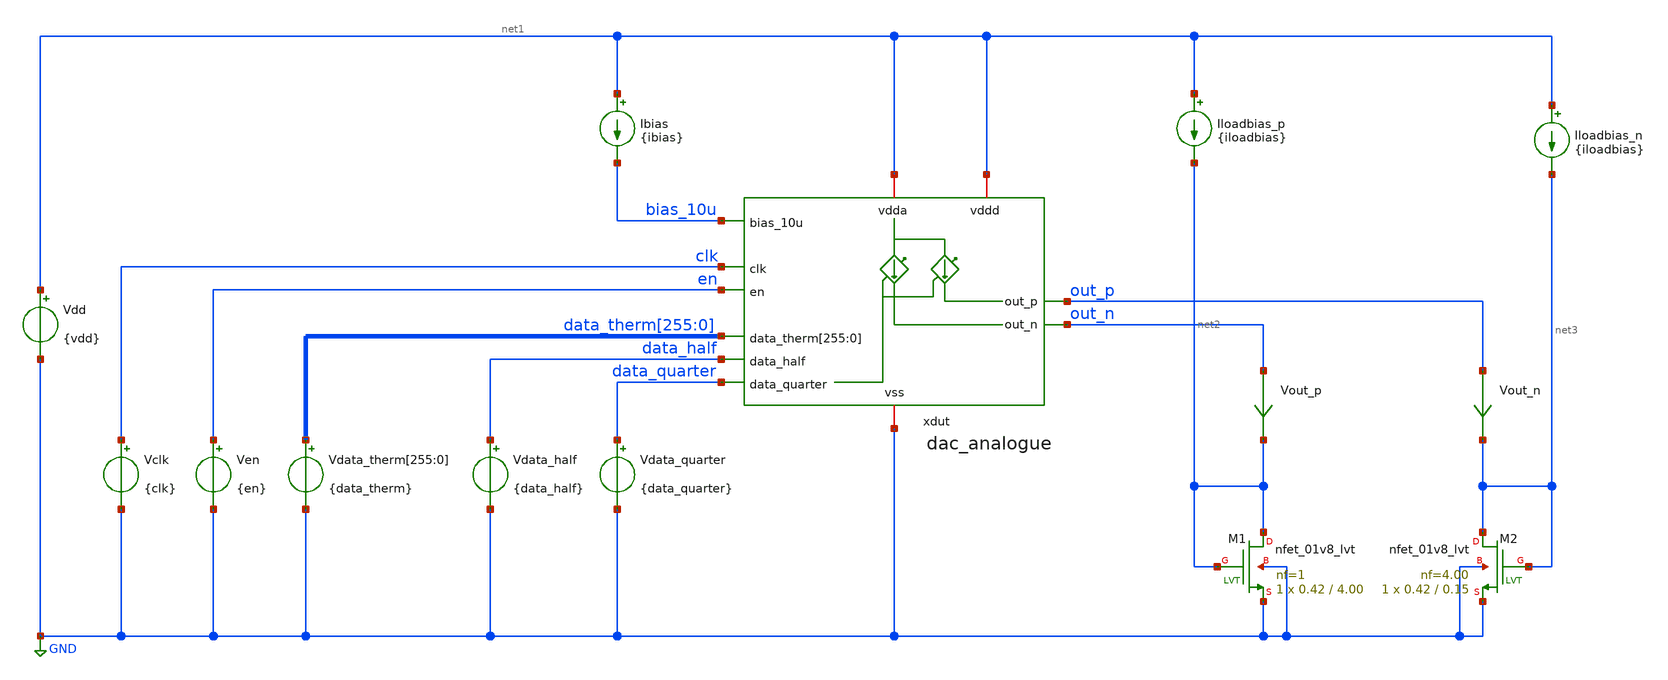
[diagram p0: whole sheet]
** sch_path: design/dac_analogue/test/dac_analogue_tb.sch
**.subckt dac_analogue_tb
Ibias net1 bias_10u {ibias}
Vdata_quarter data_quarter GND {data_quarter}
Vdata_half data_half GND {data_half}
Vdata_therm[255] data_therm[255] GND {data_therm}
Vdata_therm[254] data_therm[254] GND {data_therm}
Vdata_therm[253] data_therm[253] GND {data_therm}
Vdata_therm[252] data_therm[252] GND {data_therm}
Vdata_therm[251] data_therm[251] GND {data_therm}
Vdata_therm[250] data_therm[250] GND {data_therm}
Vdata_therm[249] data_therm[249] GND {data_therm}
Vdata_therm[248] data_therm[248] GND {data_therm}
Vdata_therm[247] data_therm[247] GND {data_therm}
Vdata_therm[246] data_therm[246] GND {data_therm}
Vdata_therm[245] data_therm[245] GND {data_therm}
Vdata_therm[244] data_therm[244] GND {data_therm}
Vdata_therm[243] data_therm[243] GND {data_therm}
Vdata_therm[242] data_therm[242] GND {data_therm}
Vdata_therm[241] data_therm[241] GND {data_therm}
Vdata_therm[240] data_therm[240] GND {data_therm}
Vdata_therm[239] data_therm[239] GND {data_therm}
Vdata_therm[238] data_therm[238] GND {data_therm}
Vdata_therm[237] data_therm[237] GND {data_therm}
Vdata_therm[236] data_therm[236] GND {data_therm}
Vdata_therm[235] data_therm[235] GND {data_therm}
Vdata_therm[234] data_therm[234] GND {data_therm}
Vdata_therm[233] data_therm[233] GND {data_therm}
Vdata_therm[232] data_therm[232] GND {data_therm}
Vdata_therm[231] data_therm[231] GND {data_therm}
Vdata_therm[230] data_therm[230] GND {data_therm}
Vdata_therm[229] data_therm[229] GND {data_therm}
Vdata_therm[228] data_therm[228] GND {data_therm}
Vdata_therm[227] data_therm[227] GND {data_therm}
Vdata_therm[226] data_therm[226] GND {data_therm}
Vdata_therm[225] data_therm[225] GND {data_therm}
Vdata_therm[224] data_therm[224] GND {data_therm}
Vdata_therm[223] data_therm[223] GND {data_therm}
Vdata_therm[222] data_therm[222] GND {data_therm}
Vdata_therm[221] data_therm[221] GND {data_therm}
Vdata_therm[220] data_therm[220] GND {data_therm}
Vdata_therm[219] data_therm[219] GND {data_therm}
Vdata_therm[218] data_therm[218] GND {data_therm}
Vdata_therm[217] data_therm[217] GND {data_therm}
Vdata_therm[216] data_therm[216] GND {data_therm}
Vdata_therm[215] data_therm[215] GND {data_therm}
Vdata_therm[214] data_therm[214] GND {data_therm}
Vdata_therm[213] data_therm[213] GND {data_therm}
Vdata_therm[212] data_therm[212] GND {data_therm}
Vdata_therm[211] data_therm[211] GND {data_therm}
Vdata_therm[210] data_therm[210] GND {data_therm}
Vdata_therm[209] data_therm[209] GND {data_therm}
Vdata_therm[208] data_therm[208] GND {data_therm}
Vdata_therm[207] data_therm[207] GND {data_therm}
Vdata_therm[206] data_therm[206] GND {data_therm}
Vdata_therm[205] data_therm[205] GND {data_therm}
Vdata_therm[204] data_therm[204] GND {data_therm}
Vdata_therm[203] data_therm[203] GND {data_therm}
Vdata_therm[202] data_therm[202] GND {data_therm}
Vdata_therm[201] data_therm[201] GND {data_therm}
Vdata_therm[200] data_therm[200] GND {data_therm}
Vdata_therm[199] data_therm[199] GND {data_therm}
Vdata_therm[198] data_therm[198] GND {data_therm}
Vdata_therm[197] data_therm[197] GND {data_therm}
Vdata_therm[196] data_therm[196] GND {data_therm}
Vdata_therm[195] data_therm[195] GND {data_therm}
Vdata_therm[194] data_therm[194] GND {data_therm}
Vdata_therm[193] data_therm[193] GND {data_therm}
Vdata_therm[192] data_therm[192] GND {data_therm}
Vdata_therm[191] data_therm[191] GND {data_therm}
Vdata_therm[190] data_therm[190] GND {data_therm}
Vdata_therm[189] data_therm[189] GND {data_therm}
Vdata_therm[188] data_therm[188] GND {data_therm}
Vdata_therm[187] data_therm[187] GND {data_therm}
Vdata_therm[186] data_therm[186] GND {data_therm}
Vdata_therm[185] data_therm[185] GND {data_therm}
Vdata_therm[184] data_therm[184] GND {data_therm}
Vdata_therm[183] data_therm[183] GND {data_therm}
Vdata_therm[182] data_therm[182] GND {data_therm}
Vdata_therm[181] data_therm[181] GND {data_therm}
Vdata_therm[180] data_therm[180] GND {data_therm}
Vdata_therm[179] data_therm[179] GND {data_therm}
Vdata_therm[178] data_therm[178] GND {data_therm}
Vdata_therm[177] data_therm[177] GND {data_therm}
Vdata_therm[176] data_therm[176] GND {data_therm}
Vdata_therm[175] data_therm[175] GND {data_therm}
Vdata_therm[174] data_therm[174] GND {data_therm}
Vdata_therm[173] data_therm[173] GND {data_therm}
Vdata_therm[172] data_therm[172] GND {data_therm}
Vdata_therm[171] data_therm[171] GND {data_therm}
Vdata_therm[170] data_therm[170] GND {data_therm}
Vdata_therm[169] data_therm[169] GND {data_therm}
Vdata_therm[168] data_therm[168] GND {data_therm}
Vdata_therm[167] data_therm[167] GND {data_therm}
Vdata_therm[166] data_therm[166] GND {data_therm}
Vdata_therm[165] data_therm[165] GND {data_therm}
Vdata_therm[164] data_therm[164] GND {data_therm}
Vdata_therm[163] data_therm[163] GND {data_therm}
Vdata_therm[162] data_therm[162] GND {data_therm}
Vdata_therm[161] data_therm[161] GND {data_therm}
Vdata_therm[160] data_therm[160] GND {data_therm}
Vdata_therm[159] data_therm[159] GND {data_therm}
Vdata_therm[158] data_therm[158] GND {data_therm}
Vdata_therm[157] data_therm[157] GND {data_therm}
Vdata_therm[156] data_therm[156] GND {data_therm}
Vdata_therm[155] data_therm[155] GND {data_therm}
Vdata_therm[154] data_therm[154] GND {data_therm}
Vdata_therm[153] data_therm[153] GND {data_therm}
Vdata_therm[152] data_therm[152] GND {data_therm}
Vdata_therm[151] data_therm[151] GND {data_therm}
Vdata_therm[150] data_therm[150] GND {data_therm}
Vdata_therm[149] data_therm[149] GND {data_therm}
Vdata_therm[148] data_therm[148] GND {data_therm}
Vdata_therm[147] data_therm[147] GND {data_therm}
Vdata_therm[146] data_therm[146] GND {data_therm}
Vdata_therm[145] data_therm[145] GND {data_therm}
Vdata_therm[144] data_therm[144] GND {data_therm}
Vdata_therm[143] data_therm[143] GND {data_therm}
Vdata_therm[142] data_therm[142] GND {data_therm}
Vdata_therm[141] data_therm[141] GND {data_therm}
Vdata_therm[140] data_therm[140] GND {data_therm}
Vdata_therm[139] data_therm[139] GND {data_therm}
Vdata_therm[138] data_therm[138] GND {data_therm}
Vdata_therm[137] data_therm[137] GND {data_therm}
Vdata_therm[136] data_therm[136] GND {data_therm}
Vdata_therm[135] data_therm[135] GND {data_therm}
Vdata_therm[134] data_therm[134] GND {data_therm}
Vdata_therm[133] data_therm[133] GND {data_therm}
Vdata_therm[132] data_therm[132] GND {data_therm}
Vdata_therm[131] data_therm[131] GND {data_therm}
Vdata_therm[130] data_therm[130] GND {data_therm}
Vdata_therm[129] data_therm[129] GND {data_therm}
Vdata_therm[128] data_therm[128] GND {data_therm}
Vdata_therm[127] data_therm[127] GND {data_therm}
Vdata_therm[126] data_therm[126] GND {data_therm}
Vdata_therm[125] data_therm[125] GND {data_therm}
Vdata_therm[124] data_therm[124] GND {data_therm}
Vdata_therm[123] data_therm[123] GND {data_therm}
Vdata_therm[122] data_therm[122] GND {data_therm}
Vdata_therm[121] data_therm[121] GND {data_therm}
Vdata_therm[120] data_therm[120] GND {data_therm}
Vdata_therm[119] data_therm[119] GND {data_therm}
Vdata_therm[118] data_therm[118] GND {data_therm}
Vdata_therm[117] data_therm[117] GND {data_therm}
Vdata_therm[116] data_therm[116] GND {data_therm}
Vdata_therm[115] data_therm[115] GND {data_therm}
Vdata_therm[114] data_therm[114] GND {data_therm}
Vdata_therm[113] data_therm[113] GND {data_therm}
Vdata_therm[112] data_therm[112] GND {data_therm}
Vdata_therm[111] data_therm[111] GND {data_therm}
Vdata_therm[110] data_therm[110] GND {data_therm}
Vdata_therm[109] data_therm[109] GND {data_therm}
Vdata_therm[108] data_therm[108] GND {data_therm}
Vdata_therm[107] data_therm[107] GND {data_therm}
Vdata_therm[106] data_therm[106] GND {data_therm}
Vdata_therm[105] data_therm[105] GND {data_therm}
Vdata_therm[104] data_therm[104] GND {data_therm}
Vdata_therm[103] data_therm[103] GND {data_therm}
Vdata_therm[102] data_therm[102] GND {data_therm}
Vdata_therm[101] data_therm[101] GND {data_therm}
Vdata_therm[100] data_therm[100] GND {data_therm}
Vdata_therm[99] data_therm[99] GND {data_therm}
Vdata_therm[98] data_therm[98] GND {data_therm}
Vdata_therm[97] data_therm[97] GND {data_therm}
Vdata_therm[96] data_therm[96] GND {data_therm}
Vdata_therm[95] data_therm[95] GND {data_therm}
Vdata_therm[94] data_therm[94] GND {data_therm}
Vdata_therm[93] data_therm[93] GND {data_therm}
Vdata_therm[92] data_therm[92] GND {data_therm}
Vdata_therm[91] data_therm[91] GND {data_therm}
Vdata_therm[90] data_therm[90] GND {data_therm}
Vdata_therm[89] data_therm[89] GND {data_therm}
Vdata_therm[88] data_therm[88] GND {data_therm}
Vdata_therm[87] data_therm[87] GND {data_therm}
Vdata_therm[86] data_therm[86] GND {data_therm}
Vdata_therm[85] data_therm[85] GND {data_therm}
Vdata_therm[84] data_therm[84] GND {data_therm}
Vdata_therm[83] data_therm[83] GND {data_therm}
Vdata_therm[82] data_therm[82] GND {data_therm}
Vdata_therm[81] data_therm[81] GND {data_therm}
Vdata_therm[80] data_therm[80] GND {data_therm}
Vdata_therm[79] data_therm[79] GND {data_therm}
Vdata_therm[78] data_therm[78] GND {data_therm}
Vdata_therm[77] data_therm[77] GND {data_therm}
Vdata_therm[76] data_therm[76] GND {data_therm}
Vdata_therm[75] data_therm[75] GND {data_therm}
Vdata_therm[74] data_therm[74] GND {data_therm}
Vdata_therm[73] data_therm[73] GND {data_therm}
Vdata_therm[72] data_therm[72] GND {data_therm}
Vdata_therm[71] data_therm[71] GND {data_therm}
Vdata_therm[70] data_therm[70] GND {data_therm}
Vdata_therm[69] data_therm[69] GND {data_therm}
Vdata_therm[68] data_therm[68] GND {data_therm}
Vdata_therm[67] data_therm[67] GND {data_therm}
Vdata_therm[66] data_therm[66] GND {data_therm}
Vdata_therm[65] data_therm[65] GND {data_therm}
Vdata_therm[64] data_therm[64] GND {data_therm}
Vdata_therm[63] data_therm[63] GND {data_therm}
Vdata_therm[62] data_therm[62] GND {data_therm}
Vdata_therm[61] data_therm[61] GND {data_therm}
Vdata_therm[60] data_therm[60] GND {data_therm}
Vdata_therm[59] data_therm[59] GND {data_therm}
Vdata_therm[58] data_therm[58] GND {data_therm}
Vdata_therm[57] data_therm[57] GND {data_therm}
Vdata_therm[56] data_therm[56] GND {data_therm}
Vdata_therm[55] data_therm[55] GND {data_therm}
Vdata_therm[54] data_therm[54] GND {data_therm}
Vdata_therm[53] data_therm[53] GND {data_therm}
Vdata_therm[52] data_therm[52] GND {data_therm}
Vdata_therm[51] data_therm[51] GND {data_therm}
Vdata_therm[50] data_therm[50] GND {data_therm}
Vdata_therm[49] data_therm[49] GND {data_therm}
Vdata_therm[48] data_therm[48] GND {data_therm}
Vdata_therm[47] data_therm[47] GND {data_therm}
Vdata_therm[46] data_therm[46] GND {data_therm}
Vdata_therm[45] data_therm[45] GND {data_therm}
Vdata_therm[44] data_therm[44] GND {data_therm}
Vdata_therm[43] data_therm[43] GND {data_therm}
Vdata_therm[42] data_therm[42] GND {data_therm}
Vdata_therm[41] data_therm[41] GND {data_therm}
Vdata_therm[40] data_therm[40] GND {data_therm}
Vdata_therm[39] data_therm[39] GND {data_therm}
Vdata_therm[38] data_therm[38] GND {data_therm}
Vdata_therm[37] data_therm[37] GND {data_therm}
Vdata_therm[36] data_therm[36] GND {data_therm}
Vdata_therm[35] data_therm[35] GND {data_therm}
Vdata_therm[34] data_therm[34] GND {data_therm}
Vdata_therm[33] data_therm[33] GND {data_therm}
Vdata_therm[32] data_therm[32] GND {data_therm}
Vdata_therm[31] data_therm[31] GND {data_therm}
Vdata_therm[30] data_therm[30] GND {data_therm}
Vdata_therm[29] data_therm[29] GND {data_therm}
Vdata_therm[28] data_therm[28] GND {data_therm}
Vdata_therm[27] data_therm[27] GND {data_therm}
Vdata_therm[26] data_therm[26] GND {data_therm}
Vdata_therm[25] data_therm[25] GND {data_therm}
Vdata_therm[24] data_therm[24] GND {data_therm}
Vdata_therm[23] data_therm[23] GND {data_therm}
Vdata_therm[22] data_therm[22] GND {data_therm}
Vdata_therm[21] data_therm[21] GND {data_therm}
Vdata_therm[20] data_therm[20] GND {data_therm}
Vdata_therm[19] data_therm[19] GND {data_therm}
Vdata_therm[18] data_therm[18] GND {data_therm}
Vdata_therm[17] data_therm[17] GND {data_therm}
Vdata_therm[16] data_therm[16] GND {data_therm}
Vdata_therm[15] data_therm[15] GND {data_therm}
Vdata_therm[14] data_therm[14] GND {data_therm}
Vdata_therm[13] data_therm[13] GND {data_therm}
Vdata_therm[12] data_therm[12] GND {data_therm}
Vdata_therm[11] data_therm[11] GND {data_therm}
Vdata_therm[10] data_therm[10] GND {data_therm}
Vdata_therm[9] data_therm[9] GND {data_therm}
Vdata_therm[8] data_therm[8] GND {data_therm}
Vdata_therm[7] data_therm[7] GND {data_therm}
Vdata_therm[6] data_therm[6] GND {data_therm}
Vdata_therm[5] data_therm[5] GND {data_therm}
Vdata_therm[4] data_therm[4] GND {data_therm}
Vdata_therm[3] data_therm[3] GND {data_therm}
Vdata_therm[2] data_therm[2] GND {data_therm}
Vdata_therm[1] data_therm[1] GND {data_therm}
Vdata_therm[0] data_therm[0] GND {data_therm}
Ven en GND {en}
Vclk clk GND {clk}
Vdd net1 GND {vdd}
XM1 net2 net2 GND GND sky130_fd_pr__nfet_01v8_lvt L=4.00 W=0.42 nf=1 ad='int((nf+1)/2) * W/nf * 0.29'
+ as='int((nf+2)/2) * W/nf * 0.29' pd='2*int((nf+1)/2) * (W/nf + 0.29)' ps='2*int((nf+2)/2) * (W/nf + 0.29)'
+ nrd='0.29 / W' nrs='0.29 / W' sa=0 sb=0 sd=0 mult=1 m=1
XM2 net3 net3 GND GND sky130_fd_pr__nfet_01v8_lvt L=0.15 W=0.42 nf=4.00 ad='int((nf+1)/2) * W/nf * 0.29'
+ as='int((nf+2)/2) * W/nf * 0.29' pd='2*int((nf+1)/2) * (W/nf + 0.29)' ps='2*int((nf+2)/2) * (W/nf + 0.29)'
+ nrd='0.29 / W' nrs='0.29 / W' sa=0 sb=0 sd=0 mult=1 m=1
Iloadbias_p net1 net2 {iloadbias}
Iloadbias_n net1 net3 {iloadbias}
Vout_p out_n net2 0
.save i(vout_p)
Vout_n out_p net3 0
.save i(vout_n)
xdut net1 net1 bias_10u clk en data_therm[255] data_therm[254] data_therm[253] data_therm[252]
+ data_therm[251] data_therm[250] data_therm[249] data_therm[248] data_therm[247] data_therm[246] data_therm[245]
+ data_therm[244] data_therm[243] data_therm[242] data_therm[241] data_therm[240] data_therm[239] data_therm[238]
+ data_therm[237] data_therm[236] data_therm[235] data_therm[234] data_therm[233] data_therm[232] data_therm[231]
+ data_therm[230] data_therm[229] data_therm[228] data_therm[227] data_therm[226] data_therm[225] data_therm[224]
+ data_therm[223] data_therm[222] data_therm[221] data_therm[220] data_therm[219] data_therm[218] data_therm[217]
+ data_therm[216] data_therm[215] data_therm[214] data_therm[213] data_therm[212] data_therm[211] data_therm[210]
+ data_therm[209] data_therm[208] data_therm[207] data_therm[206] data_therm[205] data_therm[204] data_therm[203]
+ data_therm[202] data_therm[201] data_therm[200] data_therm[199] data_therm[198] data_therm[197] data_therm[196]
+ data_therm[195] data_therm[194] data_therm[193] data_therm[192] data_therm[191] data_therm[190] data_therm[189]
+ data_therm[188] data_therm[187] data_therm[186] data_therm[185] data_therm[184] data_therm[183] data_therm[182]
+ data_therm[181] data_therm[180] data_therm[179] data_therm[178] data_therm[177] data_therm[176] data_therm[175]
+ data_therm[174] data_therm[173] data_therm[172] data_therm[171] data_therm[170] data_therm[169] data_therm[168]
+ data_therm[167] data_therm[166] data_therm[165] data_therm[164] data_therm[163] data_therm[162] data_therm[161]
+ data_therm[160] data_therm[159] data_therm[158] data_therm[157] data_therm[156] data_therm[155] data_therm[154]
+ data_therm[153] data_therm[152] data_therm[151] data_therm[150] data_therm[149] data_therm[148] data_therm[147]
+ data_therm[146] data_therm[145] data_therm[144] data_therm[143] data_therm[142] data_therm[141] data_therm[140]
+ data_therm[139] data_therm[138] data_therm[137] data_therm[136] data_therm[135] data_therm[134] data_therm[133]
+ data_therm[132] data_therm[131] data_therm[130] data_therm[129] data_therm[128] data_therm[127] data_therm[126]
+ data_therm[125] data_therm[124] data_therm[123] data_therm[122] data_therm[121] data_therm[120] data_therm[119]
+ data_therm[118] data_therm[117] data_therm[116] data_therm[115] data_therm[114] data_therm[113] data_therm[112]
+ data_therm[111] data_therm[110] data_therm[109] data_therm[108] data_therm[107] data_therm[106] data_therm[105]
+ data_therm[104] data_therm[103] data_therm[102] data_therm[101] data_therm[100] data_therm[99] data_therm[98]
+ data_therm[97] data_therm[96] data_therm[95] data_therm[94] data_therm[93] data_therm[92] data_therm[91]
+ data_therm[90] data_therm[89] data_therm[88] data_therm[87] data_therm[86] data_therm[85] data_therm[84]
+ data_therm[83] data_therm[82] data_therm[81] data_therm[80] data_therm[79] data_therm[78] data_therm[77]
+ data_therm[76] data_therm[75] data_therm[74] data_therm[73] data_therm[72] data_therm[71] data_therm[70]
+ data_therm[69] data_therm[68] data_therm[67] data_therm[66] data_therm[65] data_therm[64] data_therm[63]
+ data_therm[62] data_therm[61] data_therm[60] data_therm[59] data_therm[58] data_therm[57] data_therm[56]
+ data_therm[55] data_therm[54] data_therm[53] data_therm[52] data_therm[51] data_therm[50] data_therm[49]
+ data_therm[48] data_therm[47] data_therm[46] data_therm[45] data_therm[44] data_therm[43] data_therm[42]
+ data_therm[41] data_therm[40] data_therm[39] data_therm[38] data_therm[37] data_therm[36] data_therm[35]
+ data_therm[34] data_therm[33] data_therm[32] data_therm[31] data_therm[30] data_therm[29] data_therm[28]
+ data_therm[27] data_therm[26] data_therm[25] data_therm[24] data_therm[23] data_therm[22] data_therm[21]
+ data_therm[20] data_therm[19] data_therm[18] data_therm[17] data_therm[16] data_therm[15] data_therm[14]
+ data_therm[13] data_therm[12] data_therm[11] data_therm[10] data_therm[9] data_therm[8] data_therm[7]
+ data_therm[6] data_therm[5] data_therm[4] data_therm[3] data_therm[2] data_therm[1] data_therm[0] data_half
+ data_quarter out_p out_n GND dac_analogue
**** begin user architecture code

.options wnflag=1
.include $::SKYWATER_MODELS/cells/nfet_01v8/sky130_fd_pr__nfet_01v8__tt.corner.spice
.include $::SKYWATER_MODELS/cells/nfet_01v8_lvt/sky130_fd_pr__nfet_01v8_lvt__tt.corner.spice
.include $::SKYWATER_MODELS/cells/pfet_01v8/sky130_fd_pr__pfet_01v8__tt.corner.spice
.include $::SKYWATER_MODELS/cells/nfet_03v3_nvt/sky130_fd_pr__nfet_03v3_nvt__tt.corner.spice
.include $::SKYWATER_MODELS/cells/nfet_05v0_nvt/sky130_fd_pr__nfet_05v0_nvt__tt.corner.spice
.include $::SKYWATER_MODELS/cells/esd_nfet_01v8/sky130_fd_pr__esd_nfet_01v8__tt.corner.spice
.include $::SKYWATER_MODELS/cells/pfet_01v8_lvt/sky130_fd_pr__pfet_01v8_lvt__tt.corner.spice
.include $::SKYWATER_MODELS/cells/pfet_01v8_hvt/sky130_fd_pr__pfet_01v8_hvt__tt.corner.spice
.include $::SKYWATER_MODELS/cells/esd_pfet_g5v0d10v5/sky130_fd_pr__esd_pfet_g5v0d10v5__tt.corner.spice
.include $::SKYWATER_MODELS/cells/pfet_g5v0d10v5/sky130_fd_pr__pfet_g5v0d10v5__tt.corner.spice
.include $::SKYWATER_MODELS/cells/pfet_g5v0d16v0/sky130_fd_pr__pfet_g5v0d16v0__tt.corner.spice
.include $::SKYWATER_MODELS/cells/nfet_g5v0d10v5/sky130_fd_pr__nfet_g5v0d10v5__tt.corner.spice
.include $::SKYWATER_MODELS/cells/nfet_g5v0d16v0/sky130_fd_pr__nfet_g5v0d16v0__tt_discrete.corner.spice
.include $::SKYWATER_MODELS/cells/esd_nfet_g5v0d10v5/sky130_fd_pr__esd_nfet_g5v0d10v5__tt.corner.spice
.include $::SKYWATER_MODELS/models/corners/tt/nonfet.spice
* Mismatch parameters
.include $::SKYWATER_MODELS/cells/nfet_01v8/sky130_fd_pr__nfet_01v8__mismatch.corner.spice
.include $::SKYWATER_MODELS/cells/pfet_01v8/sky130_fd_pr__pfet_01v8__mismatch.corner.spice
.include $::SKYWATER_MODELS/cells/nfet_01v8_lvt/sky130_fd_pr__nfet_01v8_lvt__mismatch.corner.spice
.include $::SKYWATER_MODELS/cells/pfet_01v8_lvt/sky130_fd_pr__pfet_01v8_lvt__mismatch.corner.spice
.include $::SKYWATER_MODELS/cells/pfet_01v8_hvt/sky130_fd_pr__pfet_01v8_hvt__mismatch.corner.spice
.include $::SKYWATER_MODELS/cells/nfet_g5v0d10v5/sky130_fd_pr__nfet_g5v0d10v5__mismatch.corner.spice
.include $::SKYWATER_MODELS/cells/pfet_g5v0d10v5/sky130_fd_pr__pfet_g5v0d10v5__mismatch.corner.spice
.include $::SKYWATER_MODELS/cells/nfet_05v0_nvt/sky130_fd_pr__nfet_05v0_nvt__mismatch.corner.spice
.include $::SKYWATER_MODELS/cells/nfet_03v3_nvt/sky130_fd_pr__nfet_03v3_nvt__mismatch.corner.spice
* Resistor$::SKYWATER_MODELS/Capacitor
.include $::SKYWATER_MODELS/models/r+c/res_typical__cap_typical.spice
.include $::SKYWATER_MODELS/models/r+c/res_typical__cap_typical__lin.spice
* Special cells
.include $::SKYWATER_MODELS/models/corners/tt/specialized_cells.spice
* All models
.include $::SKYWATER_MODELS/models/all.spice
* Corner
.include $::SKYWATER_MODELS/models/corners/tt/rf.spice

 [sky130_models]
**** end user architecture code
**.ends
.GLOBAL GND
.end
